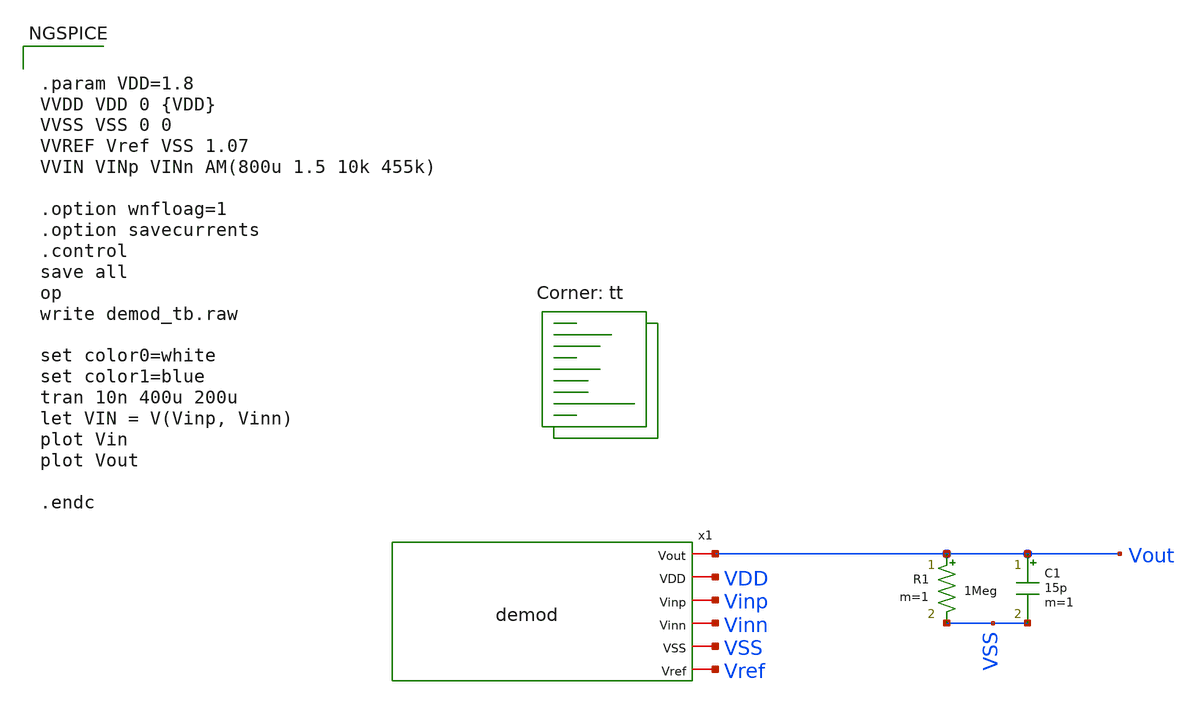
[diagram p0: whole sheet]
** sch_path: hw08/xschem/demod_tb.sch
**.subckt demod_tb
x1 Vout VDD Vinp Vinn VSS Vref demod
R1 Vout VSS 1Meg m=1
C1 Vout VSS 15p m=1
**** begin user architecture code
.lib $::SKYWATER_MODELS/sky130.lib.spice tt


.param VDD=1.8
VVDD VDD 0 {VDD}
VVSS VSS 0 0
VVREF Vref VSS 1.07
VVIN VINp VINn AM(800u 1.5 10k 455k)

.option wnfloag=1
.option savecurrents
.control
save all
op
write demod_tb.raw

set color0=white
set color1=blue
tran 10n 400u 200u
let VIN = V(Vinp, Vinn)
plot Vin
plot Vout

.endc


**** end user architecture code
**.ends

* expanding   symbol:  demod.sym # of pins=6
** sym_path: hw08/xschem/demod.sym
** sch_path: hw08/xschem/demod.sch
.subckt demod Vout VDD Vinp Vinn VSS Vref
*.iopin Vref
*.iopin VSS
*.iopin Vinn
*.iopin Vinp
*.iopin VDD
*.iopin Vout
XM1 Vp Vinp Vdiff VSS sky130_fd_pr__nfet_01v8 L=1 W=30 nf=1 ad='int((nf+1)/2) * W/nf * 0.29' as='int((nf+2)/2) * W/nf * 0.29'
+ pd='2*int((nf+1)/2) * (W/nf + 0.29)' ps='2*int((nf+2)/2) * (W/nf + 0.29)' nrd='0.29 / W' nrs='0.29 / W'
+ sa=0 sb=0 sd=0 mult=1 m=1
XM12 Vg Vinn Vdiff VSS sky130_fd_pr__nfet_01v8 L=1 W=30 nf=1 ad='int((nf+1)/2) * W/nf * 0.29' as='int((nf+2)/2) * W/nf * 0.29'
+ pd='2*int((nf+1)/2) * (W/nf + 0.29)' ps='2*int((nf+2)/2) * (W/nf + 0.29)' nrd='0.29 / W' nrs='0.29 / W'
+ sa=0 sb=0 sd=0 mult=1 m=1
XM15 Vg Vp VDD VDD sky130_fd_pr__pfet_01v8 L=1 W=30 nf=1 ad='int((nf+1)/2) * W/nf * 0.29' as='int((nf+2)/2) * W/nf * 0.29'
+ pd='2*int((nf+1)/2) * (W/nf + 0.29)' ps='2*int((nf+2)/2) * (W/nf + 0.29)' nrd='0.29 / W' nrs='0.29 / W'
+ sa=0 sb=0 sd=0 mult=1 m=1
XM13 Vp Vp VDD VDD sky130_fd_pr__pfet_01v8 L=1 W=30 nf=1 ad='int((nf+1)/2) * W/nf * 0.29' as='int((nf+2)/2) * W/nf * 0.29'
+ pd='2*int((nf+1)/2) * (W/nf + 0.29)' ps='2*int((nf+2)/2) * (W/nf + 0.29)' nrd='0.29 / W' nrs='0.29 / W'
+ sa=0 sb=0 sd=0 mult=1 m=1
XM2 Vdiff Vref VSS VSS sky130_fd_pr__nfet_01v8 L=8 W=12 nf=1 ad='int((nf+1)/2) * W/nf * 0.29' as='int((nf+2)/2) * W/nf * 0.29'
+ pd='2*int((nf+1)/2) * (W/nf + 0.29)' ps='2*int((nf+2)/2) * (W/nf + 0.29)' nrd='0.29 / W' nrs='0.29 / W'
+ sa=0 sb=0 sd=0 mult=1 m=1
XM10 Vd Vd VDD VDD sky130_fd_pr__pfet_01v8 L=1 W=30 nf=1 ad='int((nf+1)/2) * W/nf * 0.29' as='int((nf+2)/2) * W/nf * 0.29'
+ pd='2*int((nf+1)/2) * (W/nf + 0.29)' ps='2*int((nf+2)/2) * (W/nf + 0.29)' nrd='0.29 / W' nrs='0.29 / W'
+ sa=0 sb=0 sd=0 mult=1 m=1
XM11 Vdo Vd VDD VDD sky130_fd_pr__pfet_01v8 L=1 W=30 nf=1 ad='int((nf+1)/2) * W/nf * 0.29' as='int((nf+2)/2) * W/nf * 0.29'
+ pd='2*int((nf+1)/2) * (W/nf + 0.29)' ps='2*int((nf+2)/2) * (W/nf + 0.29)' nrd='0.29 / W' nrs='0.29 / W'
+ sa=0 sb=0 sd=0 mult=1 m=1
XM14 Vd Vref VSS VSS sky130_fd_pr__nfet_01v8 L=1 W=1 nf=1 ad='int((nf+1)/2) * W/nf * 0.29' as='int((nf+2)/2) * W/nf * 0.29'
+ pd='2*int((nf+1)/2) * (W/nf + 0.29)' ps='2*int((nf+2)/2) * (W/nf + 0.29)' nrd='0.29 / W' nrs='0.29 / W'
+ sa=0 sb=0 sd=0 mult=1 m=1
XM8 VSS Vg Vdo VDD sky130_fd_pr__pfet_01v8 L=1 W=30 nf=1 ad='int((nf+1)/2) * W/nf * 0.29' as='int((nf+2)/2) * W/nf * 0.29'
+ pd='2*int((nf+1)/2) * (W/nf + 0.29)' ps='2*int((nf+2)/2) * (W/nf + 0.29)' nrd='0.29 / W' nrs='0.29 / W'
+ sa=0 sb=0 sd=0 mult=1 m=1
XQ1 Vout Vout Vdo sky130_fd_pr__pnp_05v5_W3p40L3p40 m=25
XR1 VSS Vinp VSS sky130_fd_pr__res_xhigh_po_0p35 L=0.35*5 mult=1 m=1
XR2 Vinp VDD VSS sky130_fd_pr__res_xhigh_po_0p35 L=0.35*2.5 mult=1 m=1
XR3 VSS Vinn VSS sky130_fd_pr__res_xhigh_po_0p35 L=0.35*5 mult=1 m=1
XR4 Vinn VDD VSS sky130_fd_pr__res_xhigh_po_0p35 L=0.35*2.5 mult=1 m=1
.ends

.end
